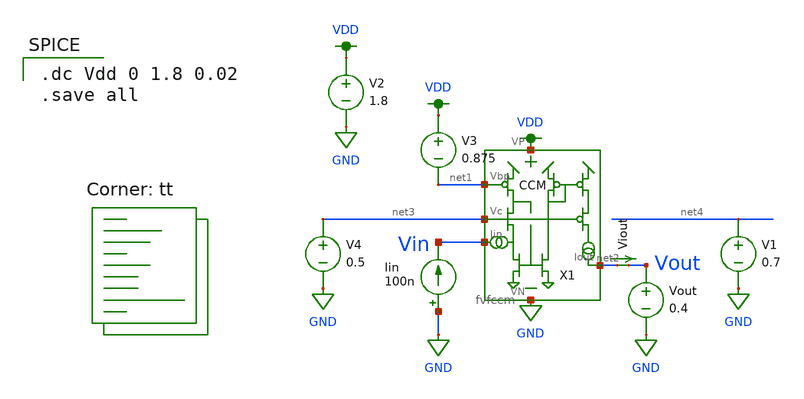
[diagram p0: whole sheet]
** sch_path: test_fvfccm_2.sch
**.subckt test_fvfccm_2
Iin GND Vin 100n
V2 VDD GND 1.8
X1 VDD net1 net3 Vin GND net2 fvfccm
V3 VDD net1 0.875
Vout Vout GND 0.4
Viout net2 Vout 0
.save i(viout)
V4 net3 GND 0.5
V1 net4 GND 0.7
**** begin user architecture code

.dc Vdd 0 1.8 0.02
.save all

.lib $::SKYWATER_MODELS/sky130.lib.spice tt
**** end user architecture code
**.ends
.GLOBAL GND
.GLOBAL VDD
.end
